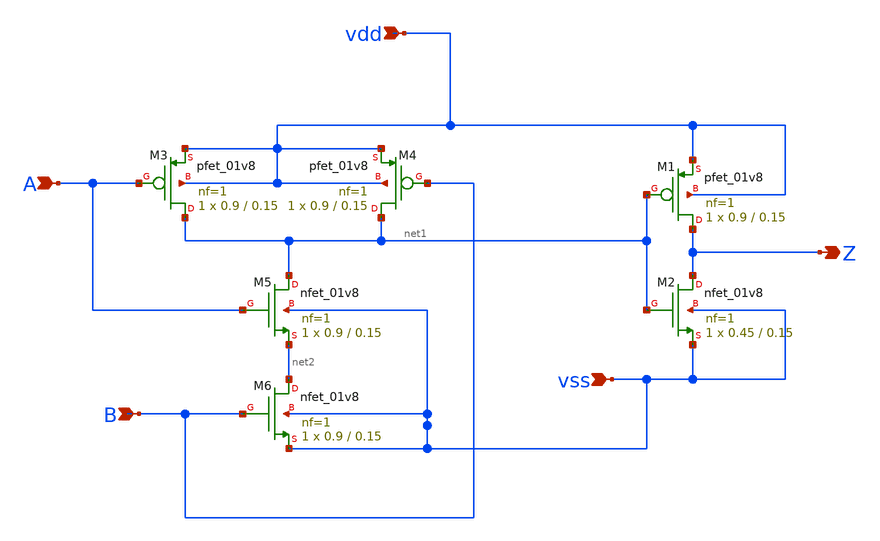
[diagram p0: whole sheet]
** sch_path: track_vlsi/lado/sch/and.sch
**.subckt and Z vdd A vss B
*.opin Z
*.ipin vdd
*.ipin A
*.ipin vss
*.ipin B
XM1 Z net1 vdd vdd sky130_fd_pr__pfet_01v8 L=0.15 W=0.9 nf=1 ad='int((nf+1)/2) * W/nf * 0.29' as='int((nf+2)/2) * W/nf * 0.29'
+ pd='2*int((nf+1)/2) * (W/nf + 0.29)' ps='2*int((nf+2)/2) * (W/nf + 0.29)' nrd='0.29 / W' nrs='0.29 / W'
+ sa=0 sb=0 sd=0 mult=1 m=1
XM2 Z net1 vss vss sky130_fd_pr__nfet_01v8 L=0.15 W=0.45 nf=1 ad='int((nf+1)/2) * W/nf * 0.29' as='int((nf+2)/2) * W/nf * 0.29'
+ pd='2*int((nf+1)/2) * (W/nf + 0.29)' ps='2*int((nf+2)/2) * (W/nf + 0.29)' nrd='0.29 / W' nrs='0.29 / W'
+ sa=0 sb=0 sd=0 mult=1 m=1
XM3 net1 A vdd vdd sky130_fd_pr__pfet_01v8 L=0.15 W=0.9 nf=1 ad='int((nf+1)/2) * W/nf * 0.29' as='int((nf+2)/2) * W/nf * 0.29'
+ pd='2*int((nf+1)/2) * (W/nf + 0.29)' ps='2*int((nf+2)/2) * (W/nf + 0.29)' nrd='0.29 / W' nrs='0.29 / W'
+ sa=0 sb=0 sd=0 mult=1 m=1
XM4 net1 B vdd vdd sky130_fd_pr__pfet_01v8 L=0.15 W=0.9 nf=1 ad='int((nf+1)/2) * W/nf * 0.29' as='int((nf+2)/2) * W/nf * 0.29'
+ pd='2*int((nf+1)/2) * (W/nf + 0.29)' ps='2*int((nf+2)/2) * (W/nf + 0.29)' nrd='0.29 / W' nrs='0.29 / W'
+ sa=0 sb=0 sd=0 mult=1 m=1
XM5 net1 A net2 vss sky130_fd_pr__nfet_01v8 L=0.15 W=0.9 nf=1 ad='int((nf+1)/2) * W/nf * 0.29' as='int((nf+2)/2) * W/nf * 0.29'
+ pd='2*int((nf+1)/2) * (W/nf + 0.29)' ps='2*int((nf+2)/2) * (W/nf + 0.29)' nrd='0.29 / W' nrs='0.29 / W'
+ sa=0 sb=0 sd=0 mult=1 m=1
XM6 net2 B vss vss sky130_fd_pr__nfet_01v8 L=0.15 W=0.9 nf=1 ad='int((nf+1)/2) * W/nf * 0.29' as='int((nf+2)/2) * W/nf * 0.29'
+ pd='2*int((nf+1)/2) * (W/nf + 0.29)' ps='2*int((nf+2)/2) * (W/nf + 0.29)' nrd='0.29 / W' nrs='0.29 / W'
+ sa=0 sb=0 sd=0 mult=1 m=1
**.ends
.end
